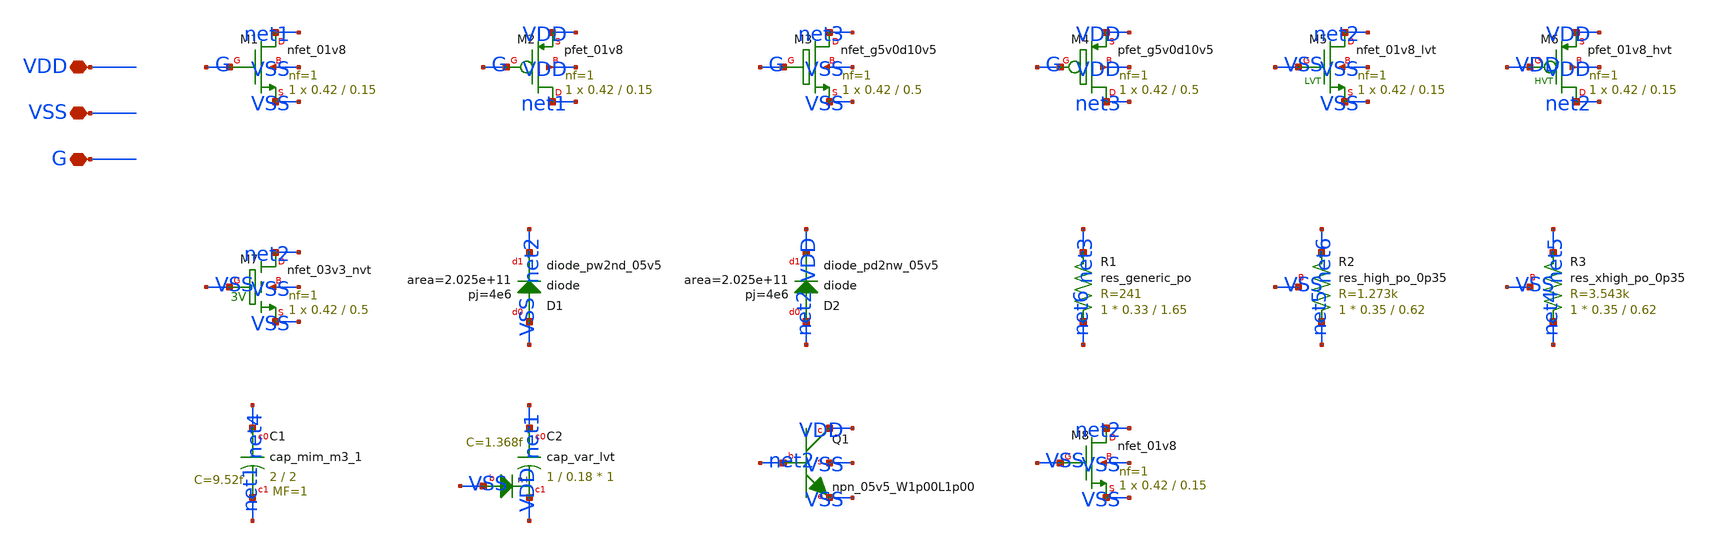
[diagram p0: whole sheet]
** sch_path: sky130A/schematic/xschem/sky130_combined.sch
**.subckt sky130_combined VDD VSS G
*.iopin VDD
*.iopin VSS
*.iopin G
XM1 net1 G VSS VSS sky130_fd_pr__nfet_01v8 L=0.15 W=0.42 nf=1 ad='int((1 + 1)/2) * 0.42 / 1 * 0.29' as='int((1 + 2)/2) * 0.42 / 1 * 0.29'
+ pd='2*int((1 + 1)/2) * (0.42 / 1 + 0.29)' ps='2*int((1 + 2)/2) * (0.42 / 1 + 0.29)' nrd='0.29 / 0.42 '
+ nrs='0.29 / 0.42 ' sa=0 sb=0 sd=0 mult=1 m=1
XM2 net1 G VDD VDD sky130_fd_pr__pfet_01v8 L=0.15 W=0.42 nf=1 ad='int((1 + 1)/2) * 0.42 / 1 * 0.29' as='int((1 + 2)/2) * 0.42 / 1 * 0.29'
+ pd='2*int((1 + 1)/2) * (0.42 / 1 + 0.29)' ps='2*int((1 + 2)/2) * (0.42 / 1 + 0.29)' nrd='0.29 / 0.42 '
+ nrs='0.29 / 0.42 ' sa=0 sb=0 sd=0 mult=1 m=1
XM3 net3 G VSS VSS sky130_fd_pr__nfet_g5v0d10v5 L=0.5 W=0.42 nf=1 ad='int((1 + 1)/2) * 0.42 / 1 * 0.29'
+ as='int((1 + 2)/2) * 0.42 / 1 * 0.29' pd='2*int((1 + 1)/2) * (0.42 / 1 + 0.29)' ps='2*int((1 + 2)/2) * (0.42 / 1 + 0.29)'
+ nrd='0.29 / 0.42 ' nrs='0.29 / 0.42 ' sa=0 sb=0 sd=0 mult=1 m=1
XM4 net3 G VDD VDD sky130_fd_pr__pfet_g5v0d10v5 L=0.5 W=0.42 nf=1 ad='int((1 + 1)/2) * 0.42 / 1 * 0.29'
+ as='int((1 + 2)/2) * 0.42 / 1 * 0.29' pd='2*int((1 + 1)/2) * (0.42 / 1 + 0.29)' ps='2*int((1 + 2)/2) * (0.42 / 1 + 0.29)'
+ nrd='0.29 / 0.42 ' nrs='0.29 / 0.42 ' sa=0 sb=0 sd=0 mult=1 m=1
XM5 net2 VSS VSS VSS sky130_fd_pr__nfet_01v8_lvt L=0.15 W=0.42 nf=1 ad='int((1 + 1)/2) * 0.42 / 1 * 0.29'
+ as='int((1 + 2)/2) * 0.42 / 1 * 0.29' pd='2*int((1 + 1)/2) * (0.42 / 1 + 0.29)' ps='2*int((1 + 2)/2) * (0.42 / 1 + 0.29)'
+ nrd='0.29 / 0.42 ' nrs='0.29 / 0.42 ' sa=0 sb=0 sd=0 mult=1 m=1
XM6 net2 VDD VDD VDD sky130_fd_pr__pfet_01v8_hvt L=0.15 W=0.42 nf=1 ad='int((1 + 1)/2) * 0.42 / 1 * 0.29'
+ as='int((1 + 2)/2) * 0.42 / 1 * 0.29' pd='2*int((1 + 1)/2) * (0.42 / 1 + 0.29)' ps='2*int((1 + 2)/2) * (0.42 / 1 + 0.29)'
+ nrd='0.29 / 0.42 ' nrs='0.29 / 0.42 ' sa=0 sb=0 sd=0 mult=1 m=1
XM7 net2 VSS VSS VSS sky130_fd_pr__nfet_03v3_nvt L=0.5 W=0.42 nf=1 ad='int((1 + 1)/2) * 0.42 / 1 * 0.29'
+ as='int((1 + 2)/2) * 0.42 / 1 * 0.29' pd='2*int((1 + 1)/2) * (0.42 / 1 + 0.29)' ps='2*int((1 + 2)/2) * (0.42 / 1 + 0.29)'
+ nrd='0.29 / 0.42 ' nrs='0.29 / 0.42 ' sa=0 sb=0 sd=0 mult=1 m=1
XD1 VSS net2 sky130_fd_pr__diode_pw2nd_05v5 area=2.025e+11 pj=4e6
XD2 net2 VDD sky130_fd_pr__diode_pd2nw_05v5 area=2.025e+11 pj=4e6
XR1 net6 net3 sky130_fd_pr__res_generic_po W=0.33 L=1.65 m=1
XR2 net5 net6 VSS sky130_fd_pr__res_high_po_0p35 L=0.62 mult=1 m=1
XR3 net4 net5 VSS sky130_fd_pr__res_xhigh_po_0p35 L=0.62 mult=1 m=1
XC1 net4 net1 sky130_fd_pr__cap_mim_m3_1 W=2 L=2 MF=1 m=1
XC2 net1 VDD VSS sky130_fd_pr__cap_var_lvt W=1 L=0.18 VM=1 m=1
XQ1 VDD net2 VSS VSS sky130_fd_pr__npn_05v5_W1p00L1p00
XM8 net2 VSS VSS VSS sky130_fd_pr__nfet_01v8 L=0.15 W=0.42 nf=1 ad='int((1 + 1)/2) * 0.42 / 1 * 0.29'
+ as='int((1 + 2)/2) * 0.42 / 1 * 0.29' pd='2*int((1 + 1)/2) * (0.42 / 1 + 0.29)' ps='2*int((1 + 2)/2) * (0.42 / 1 + 0.29)'
+ nrd='0.29 / 0.42 ' nrs='0.29 / 0.42 ' sa=0 sb=0 sd=0 mult=1 m=1
**.ends
.end
